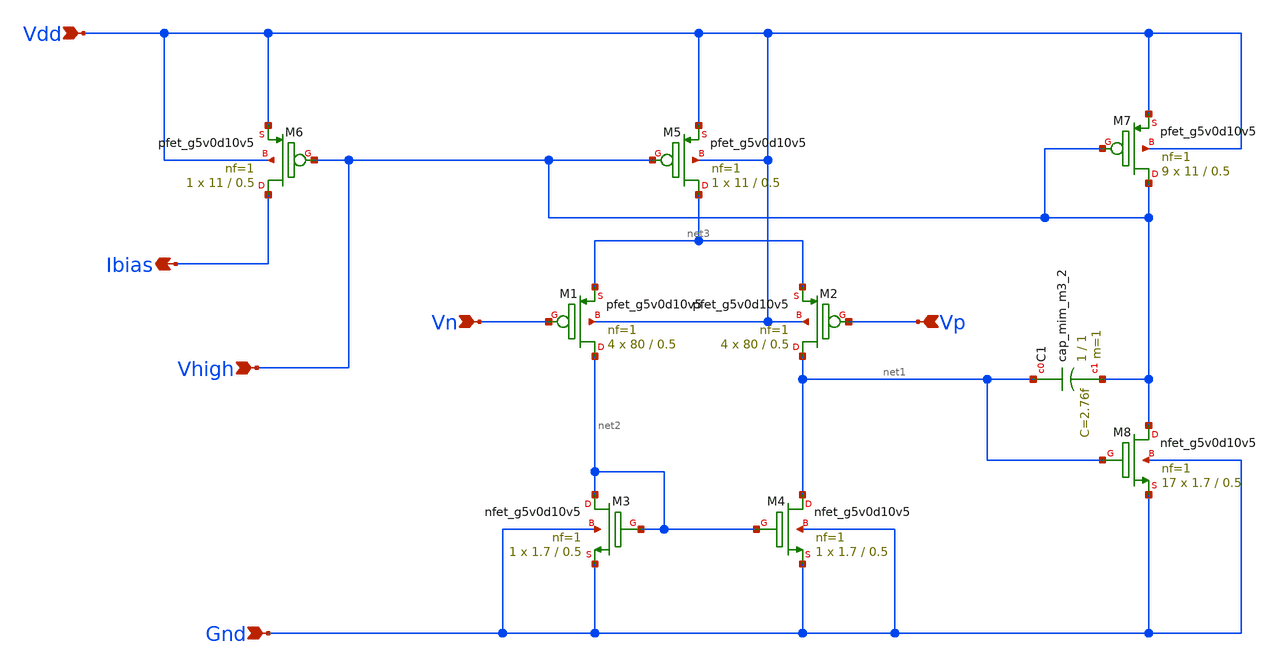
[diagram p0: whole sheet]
** sch_path: Bandgap/Schematics/BGR1.8v/Miller_OTA_1.8v.sch
**.subckt Miller_OTA_1.8v Ibias Vhigh Vdd Gnd Vp Vn
*.opin Ibias
*.ipin Vhigh
*.ipin Vdd
*.ipin Gnd
*.ipin Vp
*.ipin Vn
XM6 Ibias Vhigh Vdd Vdd sky130_fd_pr__pfet_g5v0d10v5 L=0.5 W=11 nf=1 ad='int((nf+1)/2) * W/nf * 0.29'
+ as='int((nf+2)/2) * W/nf * 0.29' pd='2*int((nf+1)/2) * (W/nf + 0.29)' ps='2*int((nf+2)/2) * (W/nf + 0.29)'
+ nrd='0.29 / W' nrs='0.29 / W' sa=0 sb=0 sd=0 mult=1 m=1
XM5 net3 Vhigh Vdd Vdd sky130_fd_pr__pfet_g5v0d10v5 L=0.5 W=11 nf=1 ad='int((nf+1)/2) * W/nf * 0.29'
+ as='int((nf+2)/2) * W/nf * 0.29' pd='2*int((nf+1)/2) * (W/nf + 0.29)' ps='2*int((nf+2)/2) * (W/nf + 0.29)'
+ nrd='0.29 / W' nrs='0.29 / W' sa=0 sb=0 sd=0 mult=1 m=1
XM7 Vhigh Vhigh Vdd Vdd sky130_fd_pr__pfet_g5v0d10v5 L=0.5 W=11 nf=1 ad='int((nf+1)/2) * W/nf * 0.29'
+ as='int((nf+2)/2) * W/nf * 0.29' pd='2*int((nf+1)/2) * (W/nf + 0.29)' ps='2*int((nf+2)/2) * (W/nf + 0.29)'
+ nrd='0.29 / W' nrs='0.29 / W' sa=0 sb=0 sd=0 mult=9 m=9
XM1 net2 Vn net3 Vdd sky130_fd_pr__pfet_g5v0d10v5 L=0.5 W=80 nf=1 ad='int((nf+1)/2) * W/nf * 0.29' as='int((nf+2)/2) * W/nf * 0.29'
+ pd='2*int((nf+1)/2) * (W/nf + 0.29)' ps='2*int((nf+2)/2) * (W/nf + 0.29)' nrd='0.29 / W' nrs='0.29 / W'
+ sa=0 sb=0 sd=0 mult=4 m=4
XM8 Vhigh net1 Gnd Gnd sky130_fd_pr__nfet_g5v0d10v5 L=0.5 W=1.7 nf=1 ad='int((nf+1)/2) * W/nf * 0.29'
+ as='int((nf+2)/2) * W/nf * 0.29' pd='2*int((nf+1)/2) * (W/nf + 0.29)' ps='2*int((nf+2)/2) * (W/nf + 0.29)'
+ nrd='0.29 / W' nrs='0.29 / W' sa=0 sb=0 sd=0 mult=17 m=17
XM4 net1 net2 Gnd Gnd sky130_fd_pr__nfet_g5v0d10v5 L=0.5 W=1.7 nf=1 ad='int((nf+1)/2) * W/nf * 0.29'
+ as='int((nf+2)/2) * W/nf * 0.29' pd='2*int((nf+1)/2) * (W/nf + 0.29)' ps='2*int((nf+2)/2) * (W/nf + 0.29)'
+ nrd='0.29 / W' nrs='0.29 / W' sa=0 sb=0 sd=0 mult=1 m=1
XM3 net2 net2 Gnd Gnd sky130_fd_pr__nfet_g5v0d10v5 L=0.5 W=1.7 nf=1 ad='int((nf+1)/2) * W/nf * 0.29'
+ as='int((nf+2)/2) * W/nf * 0.29' pd='2*int((nf+1)/2) * (W/nf + 0.29)' ps='2*int((nf+2)/2) * (W/nf + 0.29)'
+ nrd='0.29 / W' nrs='0.29 / W' sa=0 sb=0 sd=0 mult=1 m=1
XC1 net1 Vhigh sky130_fd_pr__cap_mim_m3_2 W=1 L=1 MF=1 m=1
XM2 net1 Vp net3 Vdd sky130_fd_pr__pfet_g5v0d10v5 L=0.5 W=80 nf=1 ad='int((nf+1)/2) * W/nf * 0.29' as='int((nf+2)/2) * W/nf * 0.29'
+ pd='2*int((nf+1)/2) * (W/nf + 0.29)' ps='2*int((nf+2)/2) * (W/nf + 0.29)' nrd='0.29 / W' nrs='0.29 / W'
+ sa=0 sb=0 sd=0 mult=4 m=4
**.ends
.end
